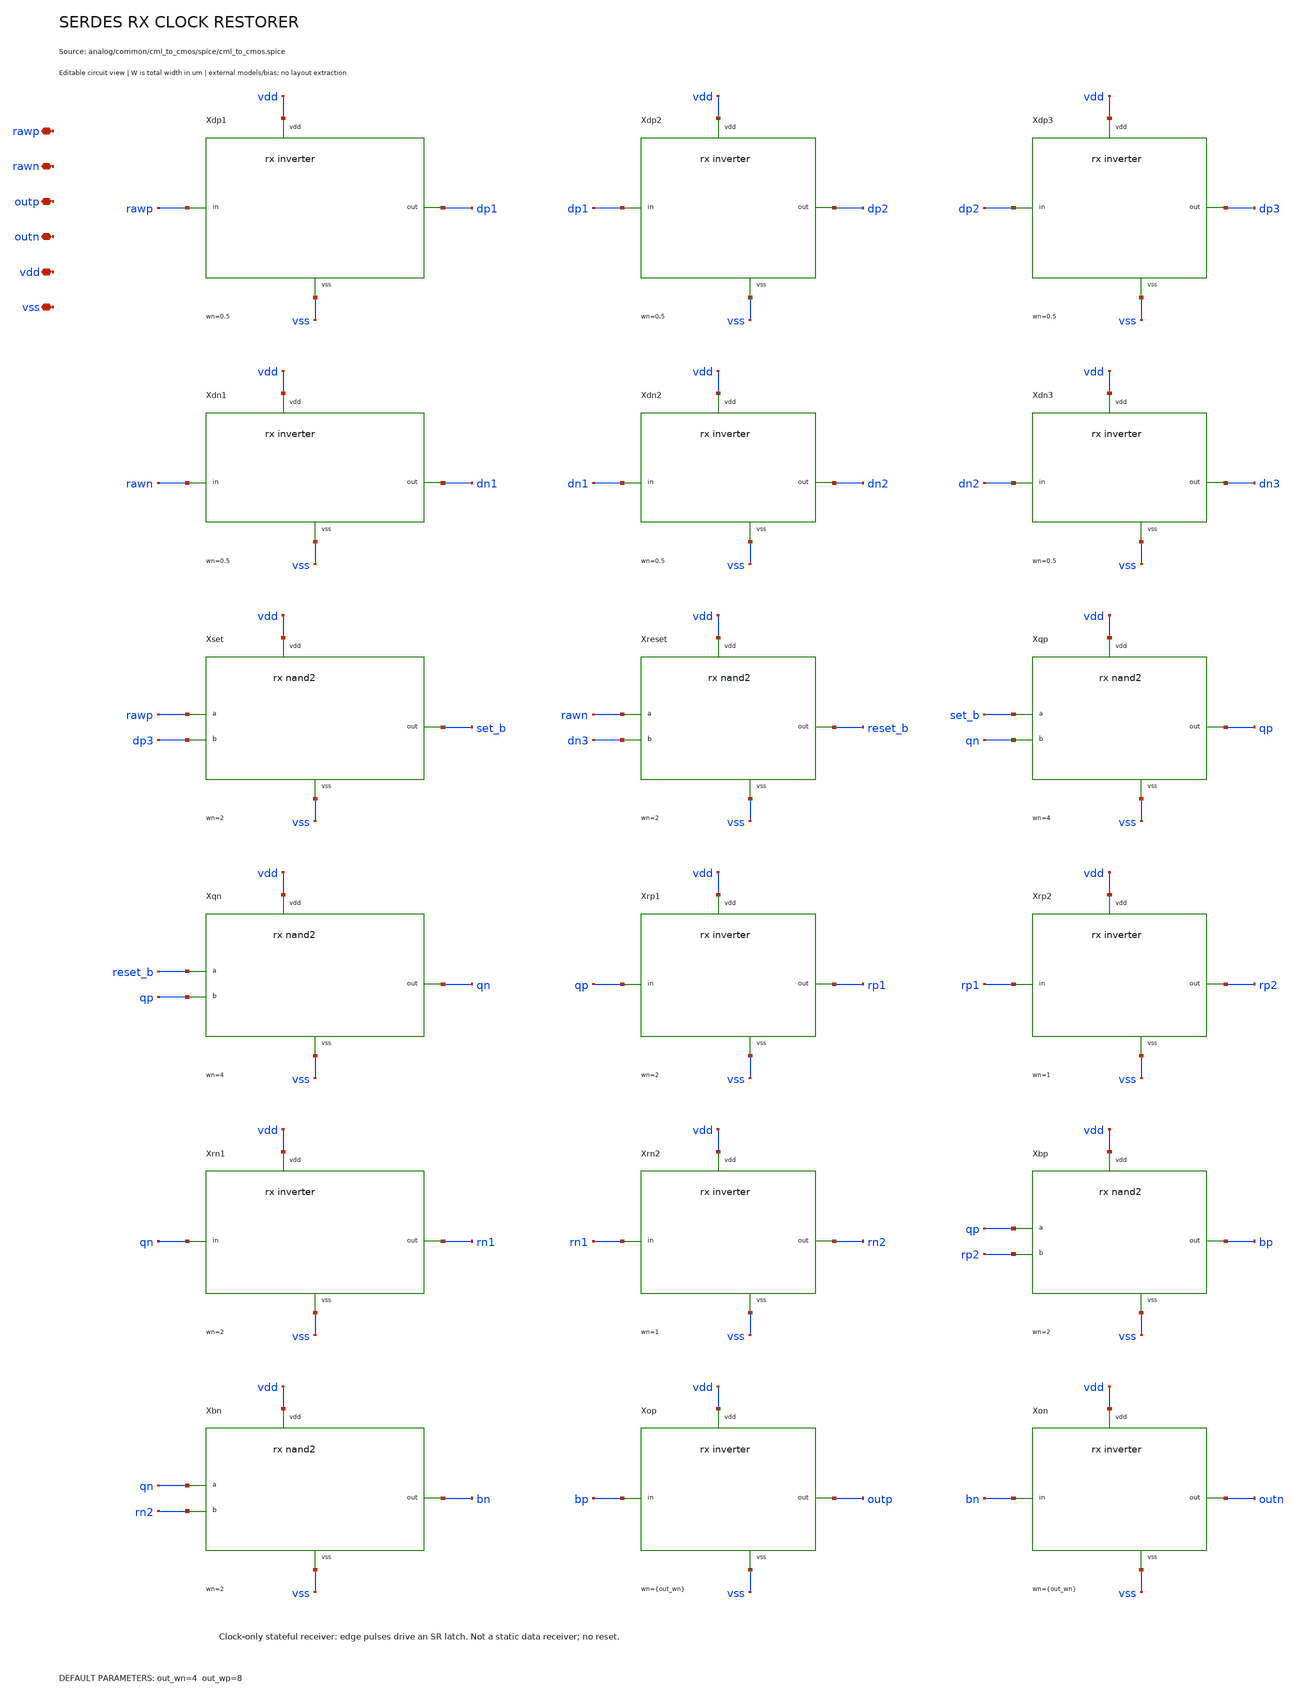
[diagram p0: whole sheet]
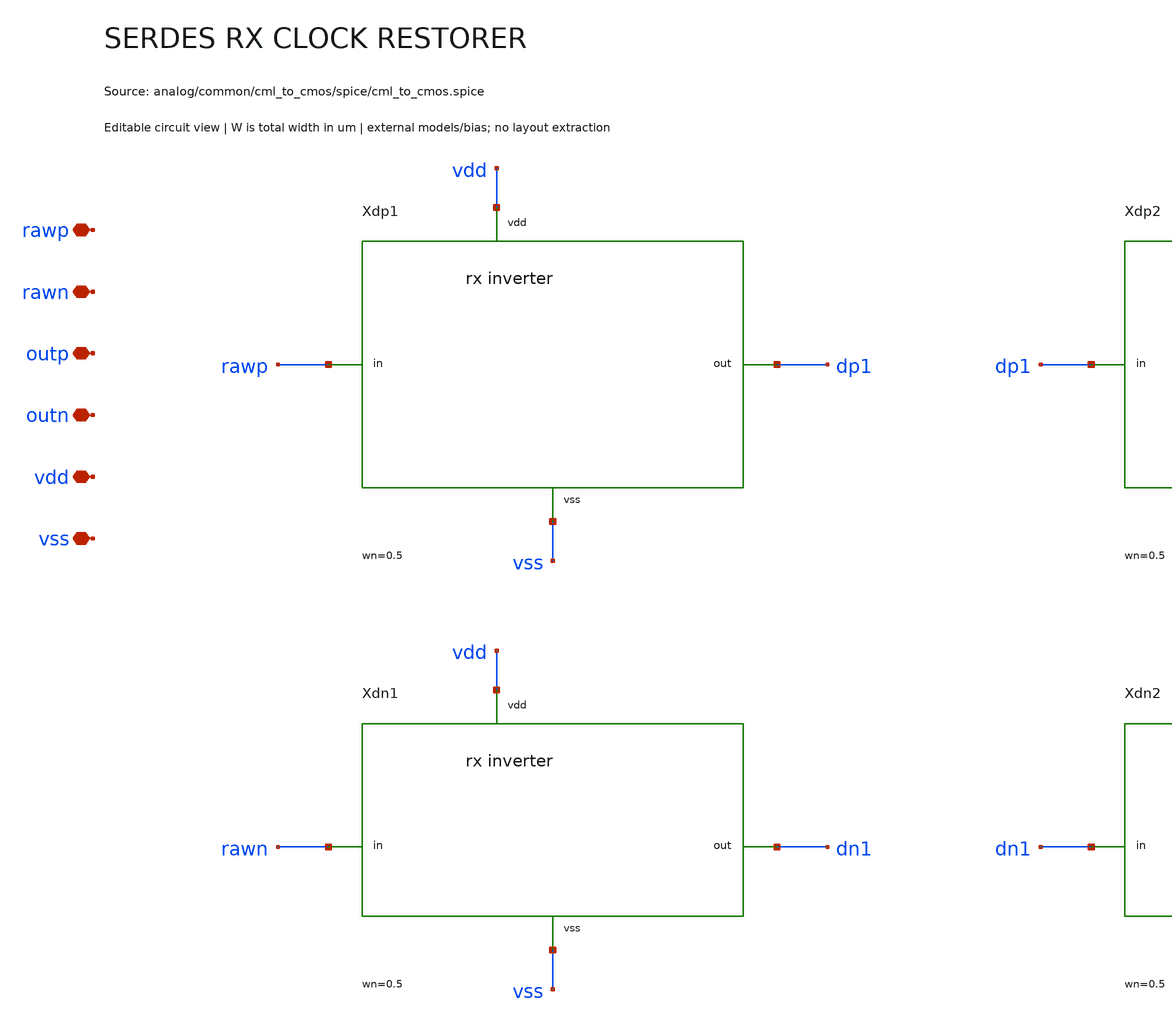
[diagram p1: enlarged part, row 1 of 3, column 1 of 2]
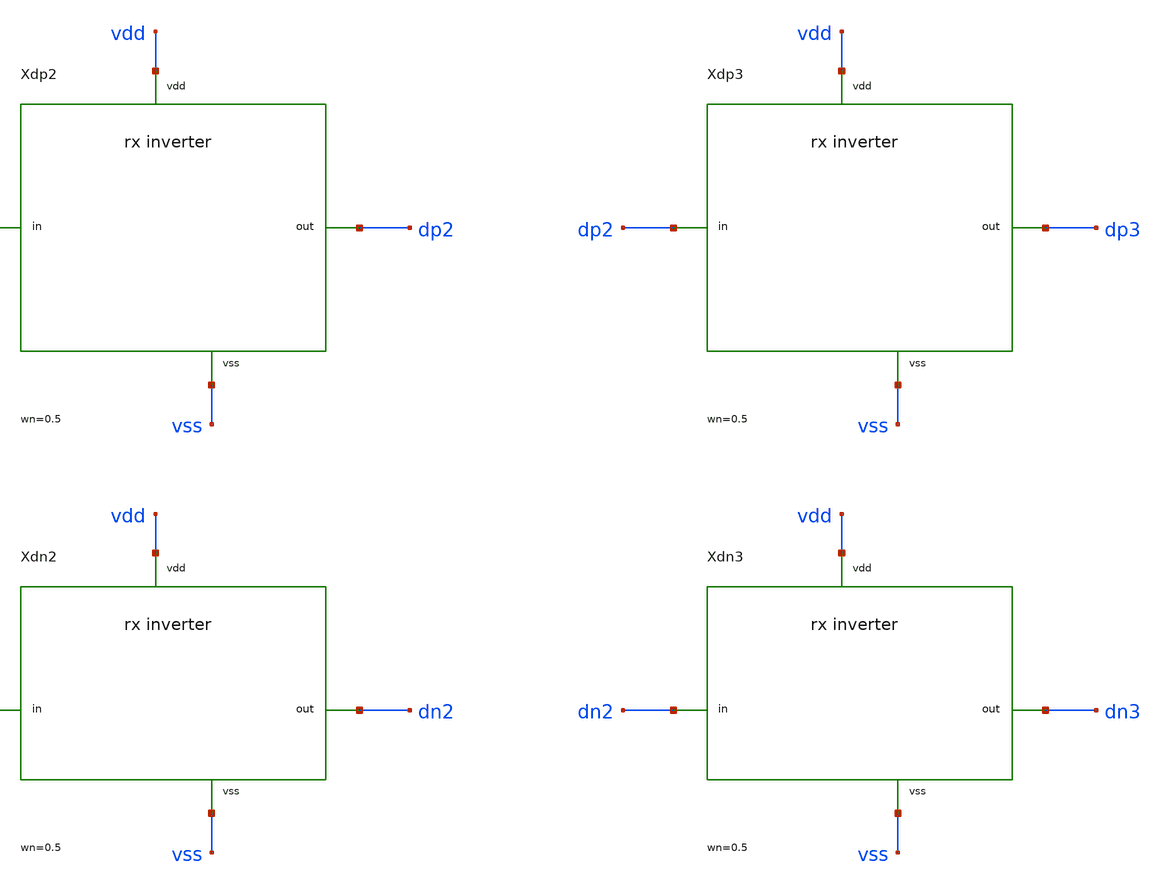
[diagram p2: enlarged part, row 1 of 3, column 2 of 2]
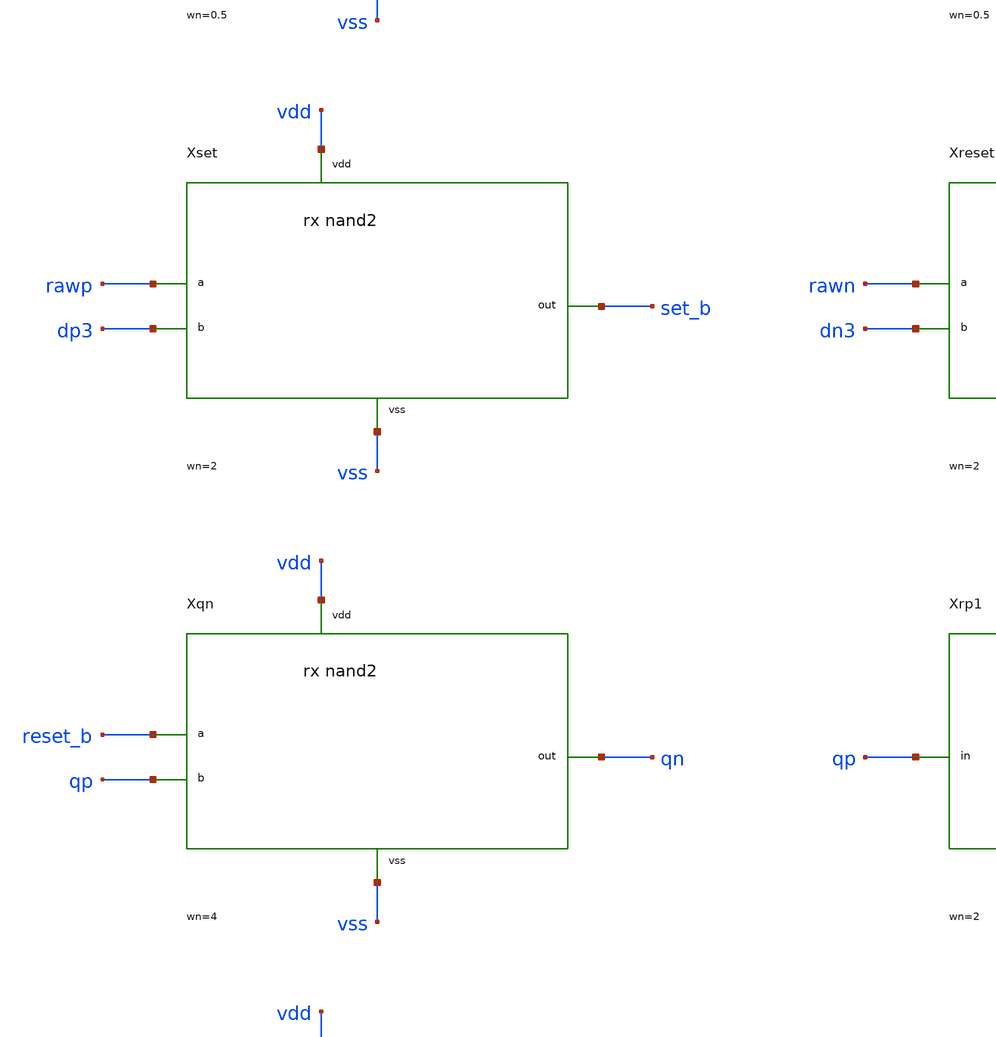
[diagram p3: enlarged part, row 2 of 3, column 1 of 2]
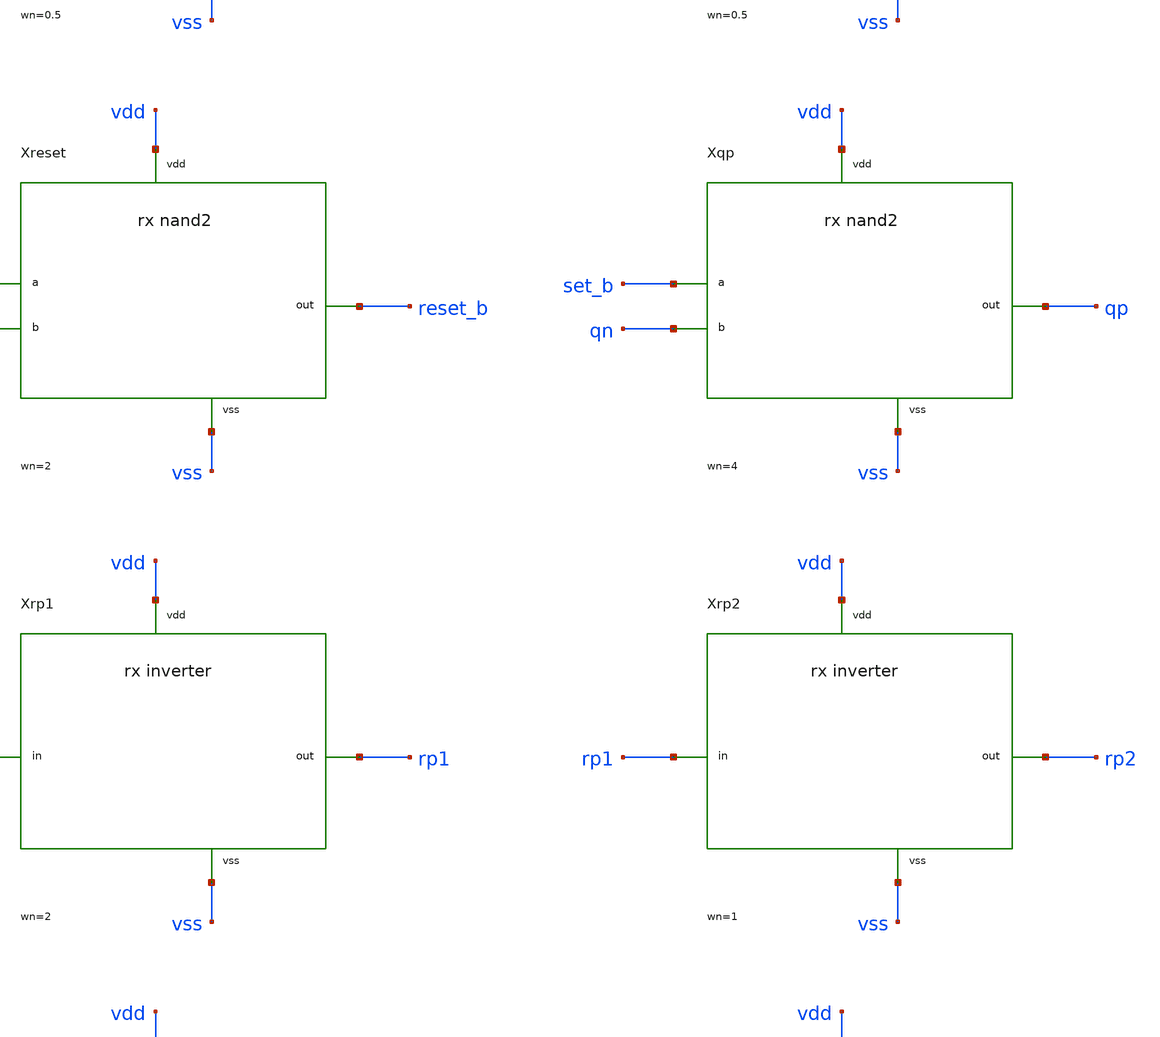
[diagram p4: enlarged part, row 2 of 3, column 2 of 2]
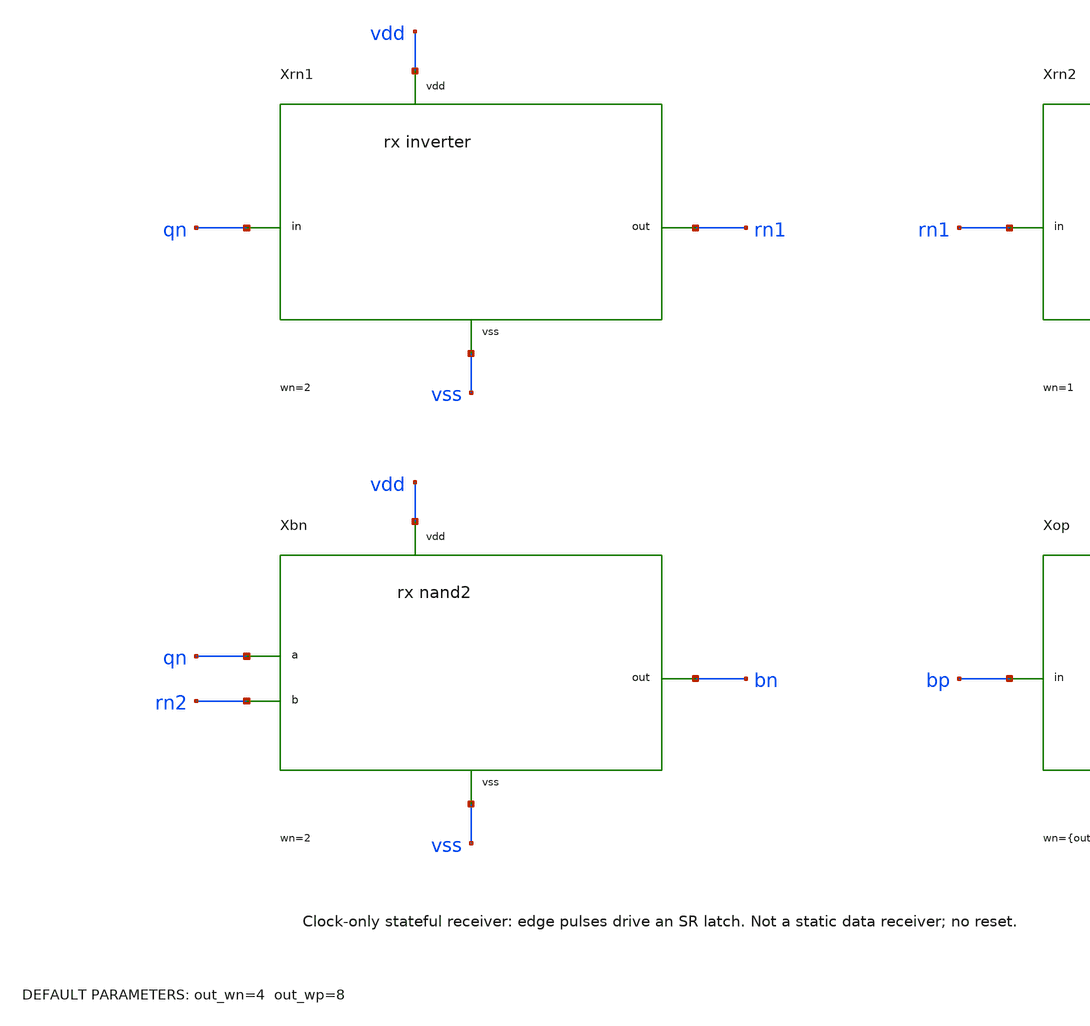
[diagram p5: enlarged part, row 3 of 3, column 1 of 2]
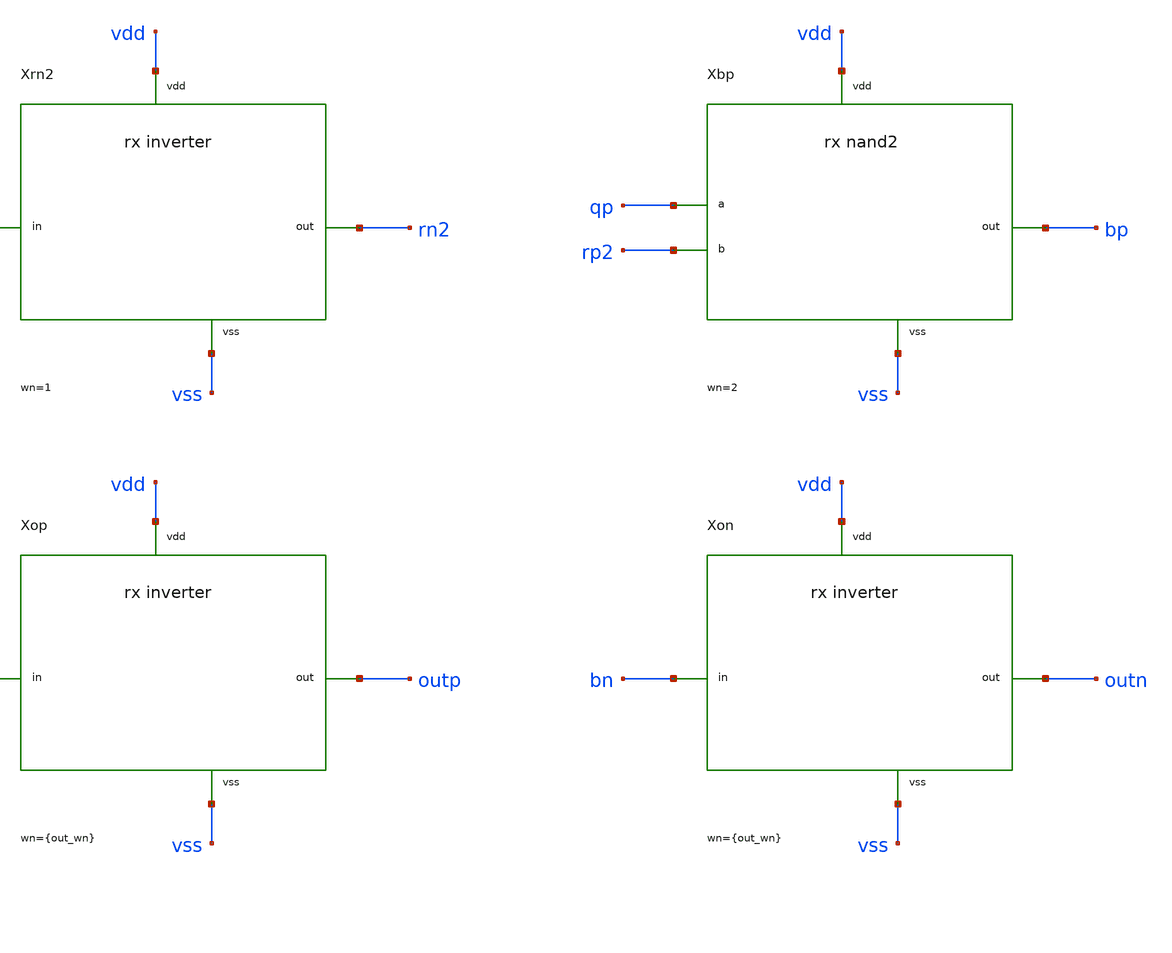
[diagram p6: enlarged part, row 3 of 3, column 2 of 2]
** sch_path: analog/common/cml_to_cmos/schematic/serdes_rx_clock_restorer.sch
**.subckt serdes_rx_clock_restorer rawp rawn outp outn vdd vss
*.iopin rawp
*.iopin rawn
*.iopin outp
*.iopin outn
*.iopin vdd
*.iopin vss
Xdp1 rawp dp1 vdd vss serdes_rx_inverter wn=0.5 wp=1.5 nfn=1 nfp=1
Xdp2 dp1 dp2 vdd vss serdes_rx_inverter wn=0.5 wp=1.5 nfn=1 nfp=1
Xdp3 dp2 dp3 vdd vss serdes_rx_inverter wn=0.5 wp=1.5 nfn=1 nfp=1
Xdn1 rawn dn1 vdd vss serdes_rx_inverter wn=0.5 wp=1.5 nfn=1 nfp=1
Xdn2 dn1 dn2 vdd vss serdes_rx_inverter wn=0.5 wp=1.5 nfn=1 nfp=1
Xdn3 dn2 dn3 vdd vss serdes_rx_inverter wn=0.5 wp=1.5 nfn=1 nfp=1
Xset rawp dp3 set_b vdd vss serdes_rx_nand2 wn=2 wp=3
Xreset rawn dn3 reset_b vdd vss serdes_rx_nand2 wn=2 wp=3
Xqp set_b qn qp vdd vss serdes_rx_nand2 wn=4 wp=6
Xqn reset_b qp qn vdd vss serdes_rx_nand2 wn=4 wp=6
Xrp1 qp rp1 vdd vss serdes_rx_inverter wn=2 wp=6 nfn=1 nfp=1
Xrp2 rp1 rp2 vdd vss serdes_rx_inverter wn=1 wp=3 nfn=1 nfp=1
Xrn1 qn rn1 vdd vss serdes_rx_inverter wn=2 wp=6 nfn=1 nfp=1
Xrn2 rn1 rn2 vdd vss serdes_rx_inverter wn=1 wp=3 nfn=1 nfp=1
Xbp qp rp2 bp vdd vss serdes_rx_nand2 wn=2 wp=3
Xbn qn rn2 bn vdd vss serdes_rx_nand2 wn=2 wp=3
Xop bp outp vdd vss serdes_rx_inverter wn={out_wn} wp={out_wp} nfn=1 nfp=4
Xon bn outn vdd vss serdes_rx_inverter wn={out_wn} wp={out_wp} nfn=1 nfp=4
**.ends

* expanding   symbol:  serdes/serdes_rx_inverter.sym # of pins=4
** sym_path: analog/common/cml_to_cmos/schematic/serdes_rx_inverter.sym
** sch_path: analog/common/cml_to_cmos/schematic/serdes_rx_inverter.sch
.subckt serdes_rx_inverter in out vdd vss  wn=1 wp=3 nfn=1 nfp=1
*.iopin in
*.iopin out
*.iopin vdd
*.iopin vss
Xn out in vss vss serdes_nfet w={wn} l=0.15 nf={nfn}
Xp out in vdd vdd serdes_pfet w={wp} l=0.15 nf={nfp}
.ends


* expanding   symbol:  serdes/serdes_rx_nand2.sym # of pins=5
** sym_path: analog/common/cml_to_cmos/schematic/serdes_rx_nand2.sym
** sch_path: analog/common/cml_to_cmos/schematic/serdes_rx_nand2.sch
.subckt serdes_rx_nand2 a b out vdd vss  wn=2 wp=3
*.iopin a
*.iopin b
*.iopin out
*.iopin vdd
*.iopin vss
Xnt out a mid vss serdes_nfet w={wn} l=0.15 nf=1
Xnb mid b vss vss serdes_nfet w={wn} l=0.15 nf=1
Xpa out a vdd vdd serdes_pfet w={wp} l=0.15 nf=1
Xpb out b vdd vdd serdes_pfet w={wp} l=0.15 nf=1
.ends


* expanding   symbol:  serdes/serdes_nfet.sym # of pins=4
** sym_path: analog/common/devices/schematic/serdes_nfet.sym
** sch_path: analog/common/devices/schematic/serdes_nfet.sch
.subckt serdes_nfet d g s b  w=1 l=0.15 nf=1
*.iopin d
*.iopin g
*.iopin s
*.iopin b
Xmos d g s b sky130_fd_pr__nfet_01v8 w={w} l={l} nf={nf} ad={floor((nf+1)/2)*(w/nf)*0.29} as={floor((nf+2)/2)*(w/nf)*0.29}
+ pd={2*floor((nf+1)/2)*(w/nf+0.29)} ps={2*floor((nf+2)/2)*(w/nf+0.29)}
.ends


* expanding   symbol:  serdes/serdes_pfet.sym # of pins=4
** sym_path: analog/common/devices/schematic/serdes_pfet.sym
** sch_path: analog/common/devices/schematic/serdes_pfet.sch
.subckt serdes_pfet d g s b  w=3 l=0.15 nf=1
*.iopin d
*.iopin g
*.iopin s
*.iopin b
Xmos d g s b sky130_fd_pr__pfet_01v8 w={w} l={l} nf={nf} ad={floor((nf+1)/2)*(w/nf)*0.29} as={floor((nf+2)/2)*(w/nf)*0.29}
+ pd={2*floor((nf+1)/2)*(w/nf+0.29)} ps={2*floor((nf+2)/2)*(w/nf+0.29)}
.ends

.end
